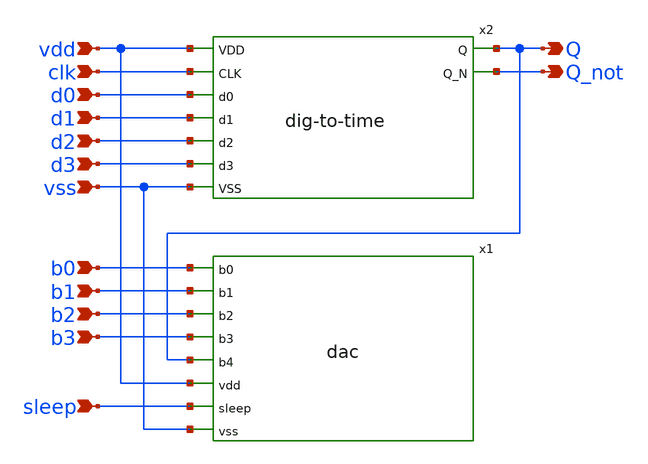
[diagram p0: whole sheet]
** sch_path: design/LELO_TORD_SKY130A/TB_dac.sch
**.subckt TB_dac b0 b1 b2 b3 sleep vss d3 d2 d1 d0 clk Q_not Q vdd
*.ipin b0
*.ipin b1
*.ipin b2
*.ipin b3
*.ipin sleep
*.ipin vss
*.ipin d3
*.ipin d2
*.ipin d1
*.ipin d0
*.ipin clk
*.opin Q_not
*.opin Q
*.ipin vdd
x1 b0 b1 b2 b3 Q vdd sleep vss dac
x2 vdd clk d0 d1 d2 d3 vss Q Q_not dig-to-time
**.ends
.end
